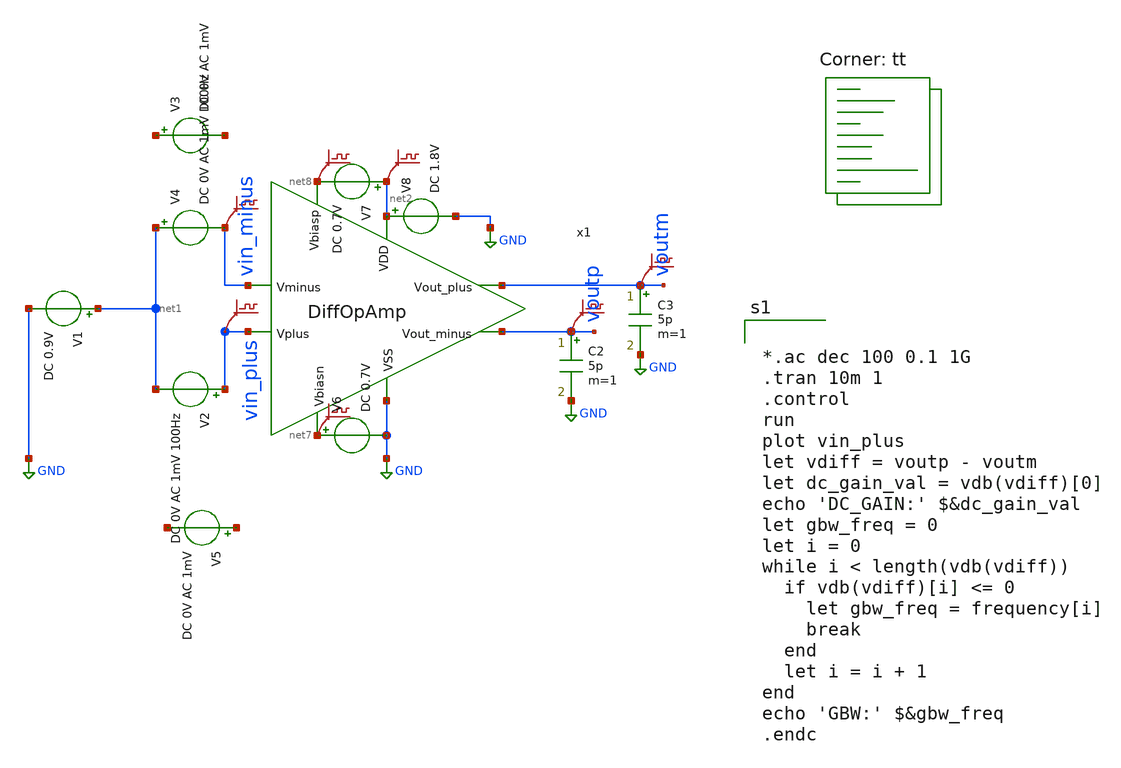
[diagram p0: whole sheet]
** sch_path: analog/library/DAC/Custom/testbenches/DiffOpAmp-tb.sch
**.subckt DiffOpAmp-tb
V1 net1 GND DC 0.9V
V3 net3 net4 DC 0V AC 1mV
V5 net5 net6 DC 0V AC 1mV
V6 net7 GND DC 0.7V
V7 net2 net8 DC 0.7V
V8 net2 GND DC 1.8V
C2 voutp GND 5p m=1
C3 voutm GND 5p m=1
x1 net2 net8 voutm voutp vin_minus vin_plus net7 GND DiffOpAmp
.save v(vin_minus)
.save v(vin_plus)
.save v(net8)
.save v(net2)
.save v(net7)
.save v(voutp)
.save v(voutm)
V2 vin_plus net1 DC 0V AC 1mV 100Hz
V4 net1 vin_minus DC 0V AC 1mV 100Hz
**** begin user architecture code


*.ac dec 100 0.1 1G
.tran 10m 1
.control
run
plot vin_plus
let vdiff = voutp - voutm
let dc_gain_val = vdb(vdiff)[0]
echo 'DC_GAIN:' $&dc_gain_val
let gbw_freq = 0
let i = 0
while i < length(vdb(vdiff))
  if vdb(vdiff)[i] <= 0
    let gbw_freq = frequency[i]
    break
  end
  let i = i + 1
end
echo 'GBW:' $&gbw_freq
.endc


.lib $::SKYWATER_MODELS/sky130.lib.spice tt
**** end user architecture code
**.ends
.GLOBAL GND
.end
